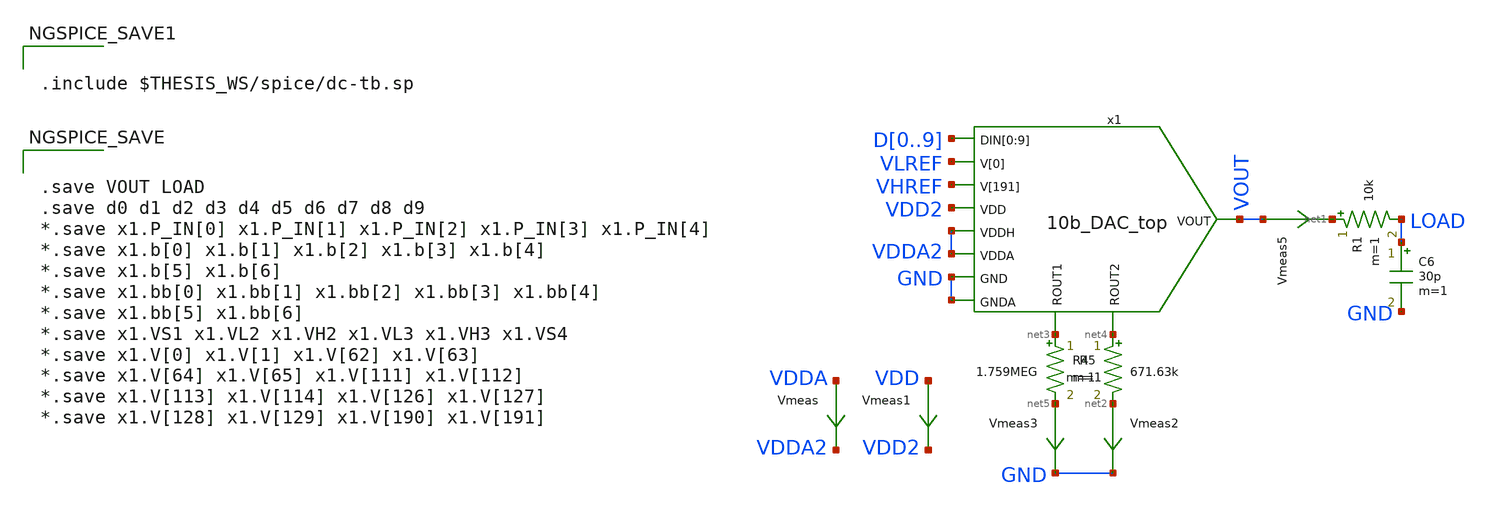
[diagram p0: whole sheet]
** sch_path: xschem/10b_DAC_dc-tb.sch
.lib $::SKYWATER_MODELS/sky130.lib.spice tt
.include $::SKYWATER_STDCELLS/sky130_fd_sc_hd.spice
.include ~/pdk/sky130A/libs.ref/sky130_fd_sc_hvl/spice/sky130_fd_sc_hvl.spice

**.subckt 10b_DAC_dc-tb
C6 LOAD GND 30p m=1
R1 net1 LOAD 10k m=1
Vmeas1 VDD VDD2 0
.save i(vmeas1)
Vmeas VDDA VDDA2 0
.save i(vmeas)
Vmeas2 net2 GND 0
.save i(vmeas2)
x1 D0 D1 D2 D3 D4 D5 D6 D7 D8 D9 VLREF VHREF VDD2 VDDA2 VDDA2 GND GND VOUT net3 net4 10b_DAC_top
Vmeas3 net5 GND 0
.save i(vmeas3)
Vmeas5 VOUT net1 0
.save i(vmeas5)
R4 net3 net5 1.759MEG m=1
R5 net4 net2 671.63k m=1
**** begin user architecture code


.save VOUT LOAD
.save d0 d1 d2 d3 d4 d5 d6 d7 d8 d9
*.save x1.P_IN[0] x1.P_IN[1] x1.P_IN[2] x1.P_IN[3] x1.P_IN[4]
*.save x1.b[0] x1.b[1] x1.b[2] x1.b[3] x1.b[4]
*.save x1.b[5] x1.b[6]
*.save x1.bb[0] x1.bb[1] x1.bb[2] x1.bb[3] x1.bb[4]
*.save x1.bb[5] x1.bb[6]
*.save x1.VS1 x1.VL2 x1.VH2 x1.VL3 x1.VH3 x1.VS4
*.save x1.V[0] x1.V[1] x1.V[62] x1.V[63]
*.save x1.V[64] x1.V[65] x1.V[111] x1.V[112]
*.save x1.V[113] x1.V[114] x1.V[126] x1.V[127]
*.save x1.V[128] x1.V[129] x1.V[190] x1.V[191]




.include $THESIS_WS/spice/dc-tb.sp


**** end user architecture code
**.ends
.end
